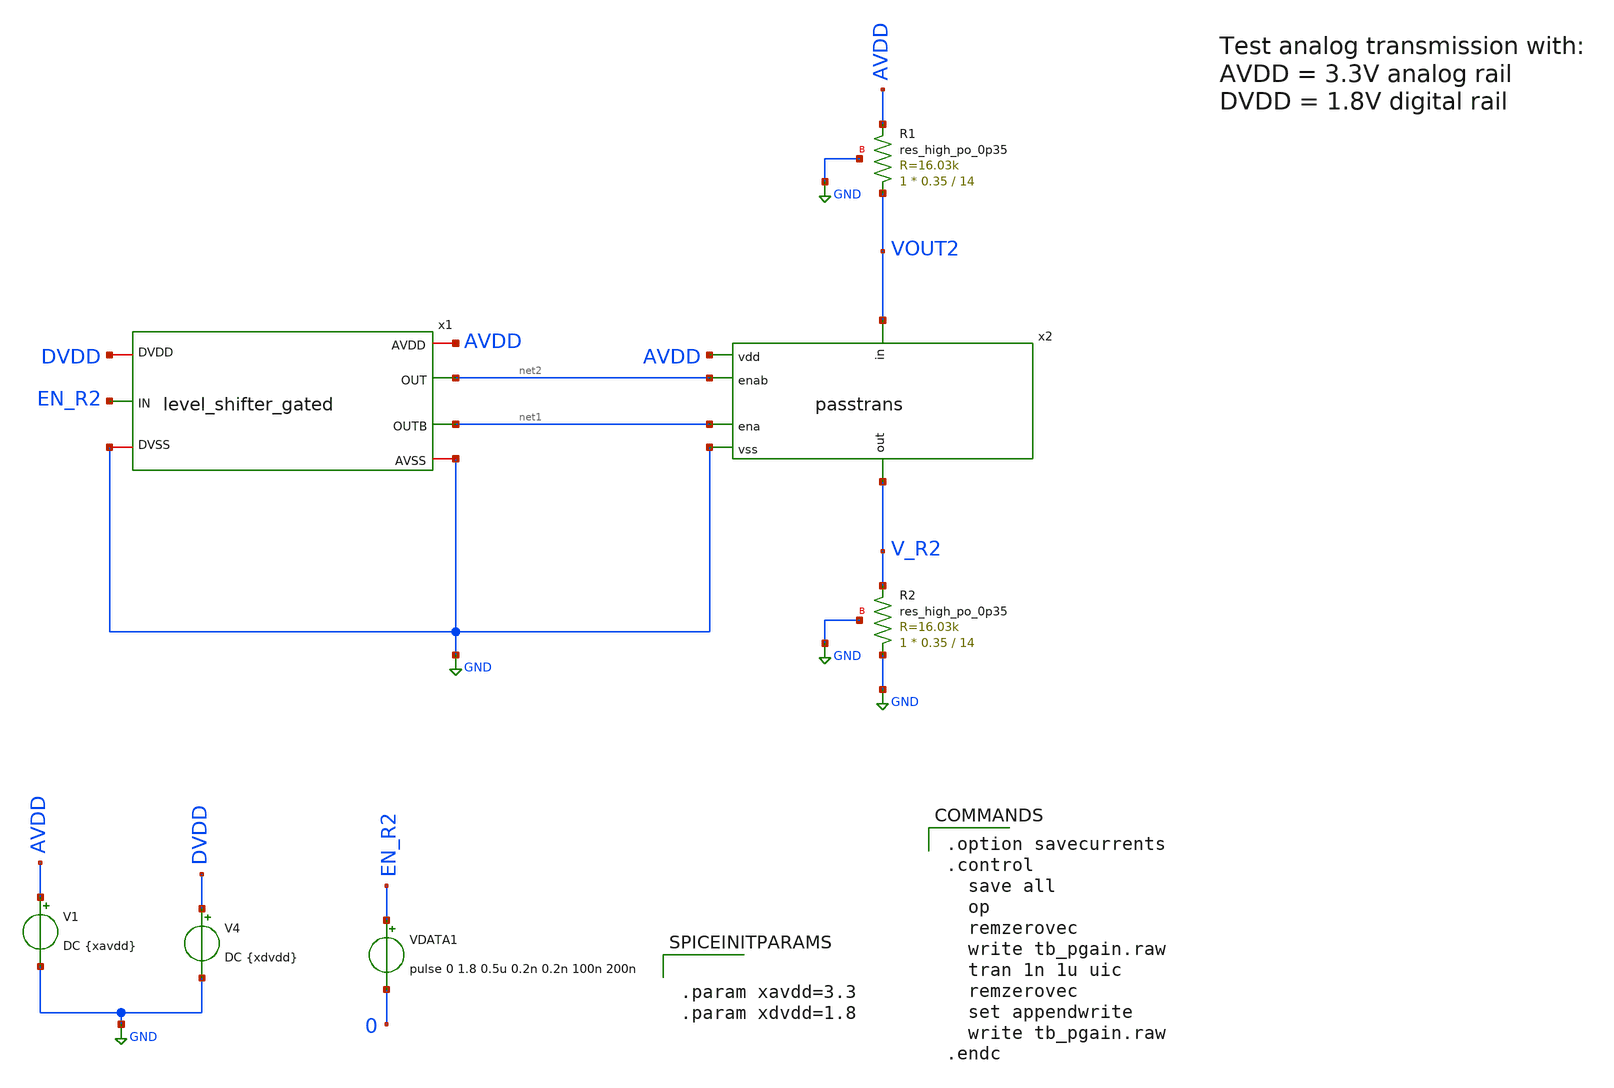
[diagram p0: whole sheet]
** sch_path: tb_pgain.sch
**.subckt tb_pgain
V1 AVDD GND DC {xavdd}
V4 DVDD GND DC {xdvdd}
x2 AVDD net2 V_R2 VOUT2 net1 GND passtrans
XR1 VOUT2 AVDD GND sky130_fd_pr__res_high_po_0p35 L=14 mult=1 m=1
XR2 GND V_R2 GND sky130_fd_pr__res_high_po_0p35 L=14 mult=1 m=1
VDATA1 EN_R2 0 pulse 0 1.8 0.5u 0.2n 0.2n 100n 200n
x1 EN_R2 DVDD net2 AVDD net1 GND GND level_shifter_gated
**** begin user architecture code


.param xavdd=3.3
.param xdvdd=1.8



** opencircuitdesign pdks install
.lib $::SKYWATER_MODELS/sky130.lib.spice tt



.option savecurrents
.control
  save all
  op
  remzerovec
  write tb_pgain.raw
  tran 1n 1u uic
  remzerovec
  set appendwrite
  write tb_pgain.raw
.endc


**** end user architecture code
**.ends

* expanding   symbol:  passtrans.sym # of pins=6
** sym_path: passtrans.sym
** sch_path: passtrans.sch
.subckt passtrans vdd enab out in ena vss
*.ipin enab
*.ipin ena
*.ipin vss
*.ipin vdd
*.ipin in
*.opin out
XM1 in ena out vss sky130_fd_pr__nfet_g5v0d10v5 L=0.5 W=10 nf=1 ad='int((nf+1)/2) * W/nf * 0.29' as='int((nf+2)/2) * W/nf * 0.29'
+ pd='2*int((nf+1)/2) * (W/nf + 0.29)' ps='2*int((nf+2)/2) * (W/nf + 0.29)' nrd='0.29 / W' nrs='0.29 / W'
+ sa=0 sb=0 sd=0 mult=1 m=1
XM2 in enab out vdd sky130_fd_pr__pfet_g5v0d10v5 L=0.5 W=10 nf=1 ad='int((nf+1)/2) * W/nf * 0.29' as='int((nf+2)/2) * W/nf * 0.29'
+ pd='2*int((nf+1)/2) * (W/nf + 0.29)' ps='2*int((nf+2)/2) * (W/nf + 0.29)' nrd='0.29 / W' nrs='0.29 / W'
+ sa=0 sb=0 sd=0 mult=1 m=1
.ends


* expanding   symbol:  level_shifter_gated.sym # of pins=7
** sym_path: level_shifter_gated.sym
** sch_path: level_shifter_gated.sch
.subckt level_shifter_gated IN DVDD OUT AVDD OUTB DVSS AVSS
*.iopin DVDD
*.iopin AVDD
*.iopin DVSS
*.iopin AVSS
*.opin OUT
*.opin OUTB
*.ipin IN
XM7 inv IN DVDD DVDD sky130_fd_pr__pfet_01v8 L=0.15 W=1 nf=1 ad='int((nf+1)/2) * W/nf * 0.29' as='int((nf+2)/2) * W/nf * 0.29'
+ pd='2*int((nf+1)/2) * (W/nf + 0.29)' ps='2*int((nf+2)/2) * (W/nf + 0.29)' nrd='0.29 / W' nrs='0.29 / W'
+ sa=0 sb=0 sd=0 mult=1 m=1
XM8 inv IN DVSS DVSS sky130_fd_pr__nfet_01v8 L=0.15 W=1 nf=1 ad='int((nf+1)/2) * W/nf * 0.29' as='int((nf+2)/2) * W/nf * 0.29'
+ pd='2*int((nf+1)/2) * (W/nf + 0.29)' ps='2*int((nf+2)/2) * (W/nf + 0.29)' nrd='0.29 / W' nrs='0.29 / W'
+ sa=0 sb=0 sd=0 mult=1 m=1
XM15 out_h outb_h net1 AVDD sky130_fd_pr__pfet_g5v0d10v5 L=0.5 W=0.42 nf=1 ad='int((nf+1)/2) * W/nf * 0.29'
+ as='int((nf+2)/2) * W/nf * 0.29' pd='2*int((nf+1)/2) * (W/nf + 0.29)' ps='2*int((nf+2)/2) * (W/nf + 0.29)'
+ nrd='0.29 / W' nrs='0.29 / W' sa=0 sb=0 sd=0 mult=1 m=1
XM16 outb_h out_h net2 AVDD sky130_fd_pr__pfet_g5v0d10v5 L=0.5 W=0.42 nf=1 ad='int((nf+1)/2) * W/nf * 0.29'
+ as='int((nf+2)/2) * W/nf * 0.29' pd='2*int((nf+1)/2) * (W/nf + 0.29)' ps='2*int((nf+2)/2) * (W/nf + 0.29)'
+ nrd='0.29 / W' nrs='0.29 / W' sa=0 sb=0 sd=0 mult=1 m=1
XM17 outb_h IN AVSS AVSS sky130_fd_pr__nfet_g5v0d10v5 L=0.5 W=0.42 nf=1 ad='int((nf+1)/2) * W/nf * 0.29'
+ as='int((nf+2)/2) * W/nf * 0.29' pd='2*int((nf+1)/2) * (W/nf + 0.29)' ps='2*int((nf+2)/2) * (W/nf + 0.29)'
+ nrd='0.29 / W' nrs='0.29 / W' sa=0 sb=0 sd=0 mult=1 m=1
XM18 out_h inv AVSS AVSS sky130_fd_pr__nfet_g5v0d10v5 L=0.5 W=0.42 nf=1 ad='int((nf+1)/2) * W/nf * 0.29'
+ as='int((nf+2)/2) * W/nf * 0.29' pd='2*int((nf+1)/2) * (W/nf + 0.29)' ps='2*int((nf+2)/2) * (W/nf + 0.29)'
+ nrd='0.29 / W' nrs='0.29 / W' sa=0 sb=0 sd=0 mult=1 m=1
XM19 net1 out_h AVDD AVDD sky130_fd_pr__pfet_g5v0d10v5 L=0.5 W=0.42 nf=1 ad='int((nf+1)/2) * W/nf * 0.29'
+ as='int((nf+2)/2) * W/nf * 0.29' pd='2*int((nf+1)/2) * (W/nf + 0.29)' ps='2*int((nf+2)/2) * (W/nf + 0.29)'
+ nrd='0.29 / W' nrs='0.29 / W' sa=0 sb=0 sd=0 mult=1 m=1
XM20 net2 outb_h AVDD AVDD sky130_fd_pr__pfet_g5v0d10v5 L=0.5 W=0.42 nf=1 ad='int((nf+1)/2) * W/nf * 0.29'
+ as='int((nf+2)/2) * W/nf * 0.29' pd='2*int((nf+1)/2) * (W/nf + 0.29)' ps='2*int((nf+2)/2) * (W/nf + 0.29)'
+ nrd='0.29 / W' nrs='0.29 / W' sa=0 sb=0 sd=0 mult=1 m=1
XM11 OUT out_h GND GND sky130_fd_pr__nfet_g5v0d10v5 L=0.5 W=0.42 nf=1 ad='int((nf+1)/2) * W/nf * 0.29'
+ as='int((nf+2)/2) * W/nf * 0.29' pd='2*int((nf+1)/2) * (W/nf + 0.29)' ps='2*int((nf+2)/2) * (W/nf + 0.29)'
+ nrd='0.29 / W' nrs='0.29 / W' sa=0 sb=0 sd=0 mult=1 m=1
XM12 OUT out_h AVDD AVDD sky130_fd_pr__pfet_g5v0d10v5 L=0.5 W=0.42 nf=1 ad='int((nf+1)/2) * W/nf * 0.29'
+ as='int((nf+2)/2) * W/nf * 0.29' pd='2*int((nf+1)/2) * (W/nf + 0.29)' ps='2*int((nf+2)/2) * (W/nf + 0.29)'
+ nrd='0.29 / W' nrs='0.29 / W' sa=0 sb=0 sd=0 mult=1 m=1
XM13 OUTB outb_h GND GND sky130_fd_pr__nfet_g5v0d10v5 L=0.5 W=0.42 nf=1 ad='int((nf+1)/2) * W/nf * 0.29'
+ as='int((nf+2)/2) * W/nf * 0.29' pd='2*int((nf+1)/2) * (W/nf + 0.29)' ps='2*int((nf+2)/2) * (W/nf + 0.29)'
+ nrd='0.29 / W' nrs='0.29 / W' sa=0 sb=0 sd=0 mult=1 m=1
XM14 OUTB outb_h AVDD AVDD sky130_fd_pr__pfet_g5v0d10v5 L=0.5 W=0.42 nf=1 ad='int((nf+1)/2) * W/nf * 0.29'
+ as='int((nf+2)/2) * W/nf * 0.29' pd='2*int((nf+1)/2) * (W/nf + 0.29)' ps='2*int((nf+2)/2) * (W/nf + 0.29)'
+ nrd='0.29 / W' nrs='0.29 / W' sa=0 sb=0 sd=0 mult=1 m=1
.ends

.GLOBAL GND
.end
